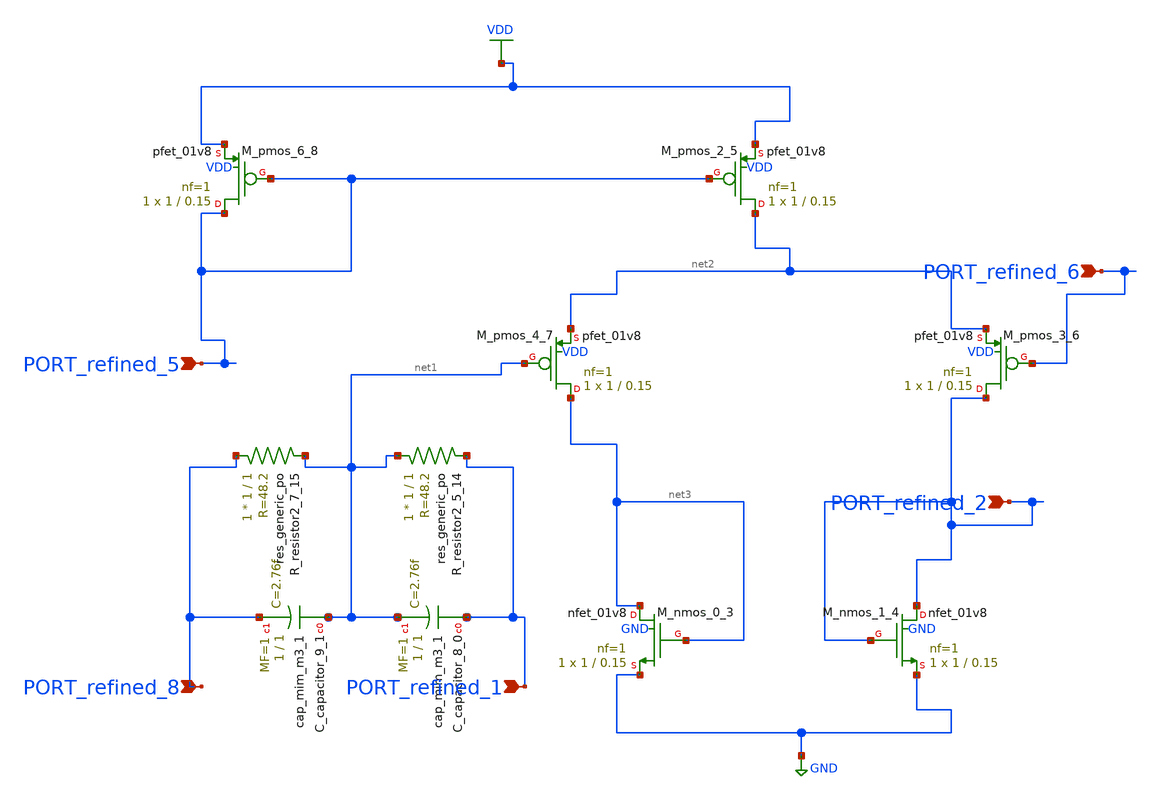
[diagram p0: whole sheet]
** sch_path: schematics/SchemGen/10_1109_TCSI_2022_3216201_04_001_crop2.sch
**.subckt 10_1109_TCSI_2022_3216201_04_001_crop2 PORT_refined_1 PORT_refined_8 PORT_refined_6
*+ PORT_refined_2 PORT_refined_5
*.ipin PORT_refined_1
*.ipin PORT_refined_8
*.ipin PORT_refined_6
*.ipin PORT_refined_2
*.ipin PORT_refined_5
XC_capacitor_8_0 PORT_refined_1 net1 sky130_fd_pr__cap_mim_m3_1 W=1 L=1 MF=1 m=1
XC_capacitor_9_1 net1 PORT_refined_8 sky130_fd_pr__cap_mim_m3_1 W=1 L=1 MF=1 m=1
XM_nmos_0_3 net3 net3 GND GND sky130_fd_pr__nfet_01v8 L=0.15 W=1 nf=1 ad='int((1 + 1)/2) * 1 / 1 * 0.29'
+ as='int((1 + 2)/2) * 1 / 1 * 0.29' pd='2*int((1 + 1)/2) * (1 / 1 + 0.29)' ps='2*int((1 + 2)/2) * (1 / 1 + 0.29)'
+ nrd='0.29 / 1 ' nrs='0.29 / 1 ' sa=0 sb=0 sd=0 mult=1 m=1
XM_nmos_1_4 PORT_refined_2 PORT_refined_2 GND GND sky130_fd_pr__nfet_01v8 L=0.15 W=1 nf=1 ad='int((1 + 1)/2) * 1 / 1 * 0.29'
+ as='int((1 + 2)/2) * 1 / 1 * 0.29' pd='2*int((1 + 1)/2) * (1 / 1 + 0.29)' ps='2*int((1 + 2)/2) * (1 / 1 + 0.29)'
+ nrd='0.29 / 1 ' nrs='0.29 / 1 ' sa=0 sb=0 sd=0 mult=1 m=1
XM_pmos_2_5 net2 PORT_refined_5 VDD VDD sky130_fd_pr__pfet_01v8 L=0.15 W=1 nf=1 ad='int((1 + 1)/2) * 1 / 1 * 0.29'
+ as='int((1 + 2)/2) * 1 / 1 * 0.29' pd='2*int((1 + 1)/2) * (1 / 1 + 0.29)' ps='2*int((1 + 2)/2) * (1 / 1 + 0.29)'
+ nrd='0.29 / 1 ' nrs='0.29 / 1 ' sa=0 sb=0 sd=0 mult=1 m=1
XM_pmos_3_6 PORT_refined_2 PORT_refined_6 net2 VDD sky130_fd_pr__pfet_01v8 L=0.15 W=1 nf=1 ad='int((1 + 1)/2) * 1 / 1 * 0.29'
+ as='int((1 + 2)/2) * 1 / 1 * 0.29' pd='2*int((1 + 1)/2) * (1 / 1 + 0.29)' ps='2*int((1 + 2)/2) * (1 / 1 + 0.29)'
+ nrd='0.29 / 1 ' nrs='0.29 / 1 ' sa=0 sb=0 sd=0 mult=1 m=1
XM_pmos_4_7 net3 net1 net2 VDD sky130_fd_pr__pfet_01v8 L=0.15 W=1 nf=1 ad='int((1 + 1)/2) * 1 / 1 * 0.29'
+ as='int((1 + 2)/2) * 1 / 1 * 0.29' pd='2*int((1 + 1)/2) * (1 / 1 + 0.29)' ps='2*int((1 + 2)/2) * (1 / 1 + 0.29)'
+ nrd='0.29 / 1 ' nrs='0.29 / 1 ' sa=0 sb=0 sd=0 mult=1 m=1
XM_pmos_6_8 PORT_refined_5 PORT_refined_5 VDD VDD sky130_fd_pr__pfet_01v8 L=0.15 W=1 nf=1 ad='int((1 + 1)/2) * 1 / 1 * 0.29'
+ as='int((1 + 2)/2) * 1 / 1 * 0.29' pd='2*int((1 + 1)/2) * (1 / 1 + 0.29)' ps='2*int((1 + 2)/2) * (1 / 1 + 0.29)'
+ nrd='0.29 / 1 ' nrs='0.29 / 1 ' sa=0 sb=0 sd=0 mult=1 m=1
XR_resistor2_5_14 net1 PORT_refined_1 sky130_fd_pr__res_generic_po W=1 L=1 m=1
XR_resistor2_7_15 PORT_refined_8 net1 sky130_fd_pr__res_generic_po W=1 L=1 m=1
**.ends
.GLOBAL GND
.GLOBAL VDD
.end
